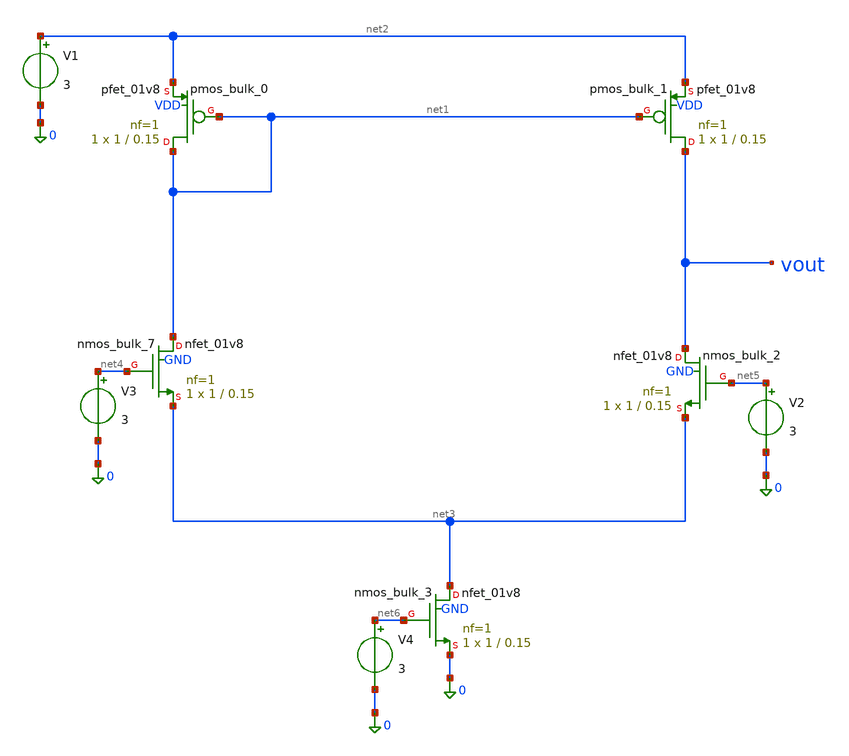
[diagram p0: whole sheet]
** sch_path: golden_netlists/10_1007_s42452-023-05572-9_09_002.sch
**.subckt 10_1007_s42452-023-05572-9_09_002
Xnmos_bulk_2 vout net5 net3 GND sky130_fd_pr__nfet_01v8 L=0.15 W=1 nf=1 ad='int((nf+1)/2) * W/nf * 0.29'
+ as='int((nf+2)/2) * W/nf * 0.29' pd='2*int((nf+1)/2) * (W/nf + 0.29)' ps='2*int((nf+2)/2) * (W/nf + 0.29)'
+ nrd='0.29 / W' nrs='0.29 / W' sa=0 sb=0 sd=0 mult=1 m=1
Xnmos_bulk_3 net3 net6 0 GND sky130_fd_pr__nfet_01v8 L=0.15 W=1 nf=1 ad='int((nf+1)/2) * W/nf * 0.29'
+ as='int((nf+2)/2) * W/nf * 0.29' pd='2*int((nf+1)/2) * (W/nf + 0.29)' ps='2*int((nf+2)/2) * (W/nf + 0.29)'
+ nrd='0.29 / W' nrs='0.29 / W' sa=0 sb=0 sd=0 mult=1 m=1
Xnmos_bulk_7 net1 net4 net3 GND sky130_fd_pr__nfet_01v8 L=0.15 W=1 nf=1 ad='int((nf+1)/2) * W/nf * 0.29'
+ as='int((nf+2)/2) * W/nf * 0.29' pd='2*int((nf+1)/2) * (W/nf + 0.29)' ps='2*int((nf+2)/2) * (W/nf + 0.29)'
+ nrd='0.29 / W' nrs='0.29 / W' sa=0 sb=0 sd=0 mult=1 m=1
Xpmos_bulk_0 net1 net1 net2 VDD sky130_fd_pr__pfet_01v8 L=0.15 W=1 nf=1 ad='int((1 + 1)/2) * 1 / 1 * 0.29'
+ as='int((1 + 2)/2) * 1 / 1 * 0.29' pd='2*int((1 + 1)/2) * (1 / 1 + 0.29)' ps='2*int((1 + 2)/2) * (1 / 1 + 0.29)'
+ nrd='0.29 / 1 ' nrs='0.29 / 1 ' sa=0 sb=0 sd=0 mult=1 m=1
Xpmos_bulk_1 vout net1 net2 VDD sky130_fd_pr__pfet_01v8 L=0.15 W=1 nf=1 ad='int((1 + 1)/2) * 1 / 1 * 0.29'
+ as='int((1 + 2)/2) * 1 / 1 * 0.29' pd='2*int((1 + 1)/2) * (1 / 1 + 0.29)' ps='2*int((1 + 2)/2) * (1 / 1 + 0.29)'
+ nrd='0.29 / 1 ' nrs='0.29 / 1 ' sa=0 sb=0 sd=0 mult=1 m=1
V1 net2 0 3
V2 net5 0 3
V3 net4 0 3
V4 net6 0 3
**.ends
.end
